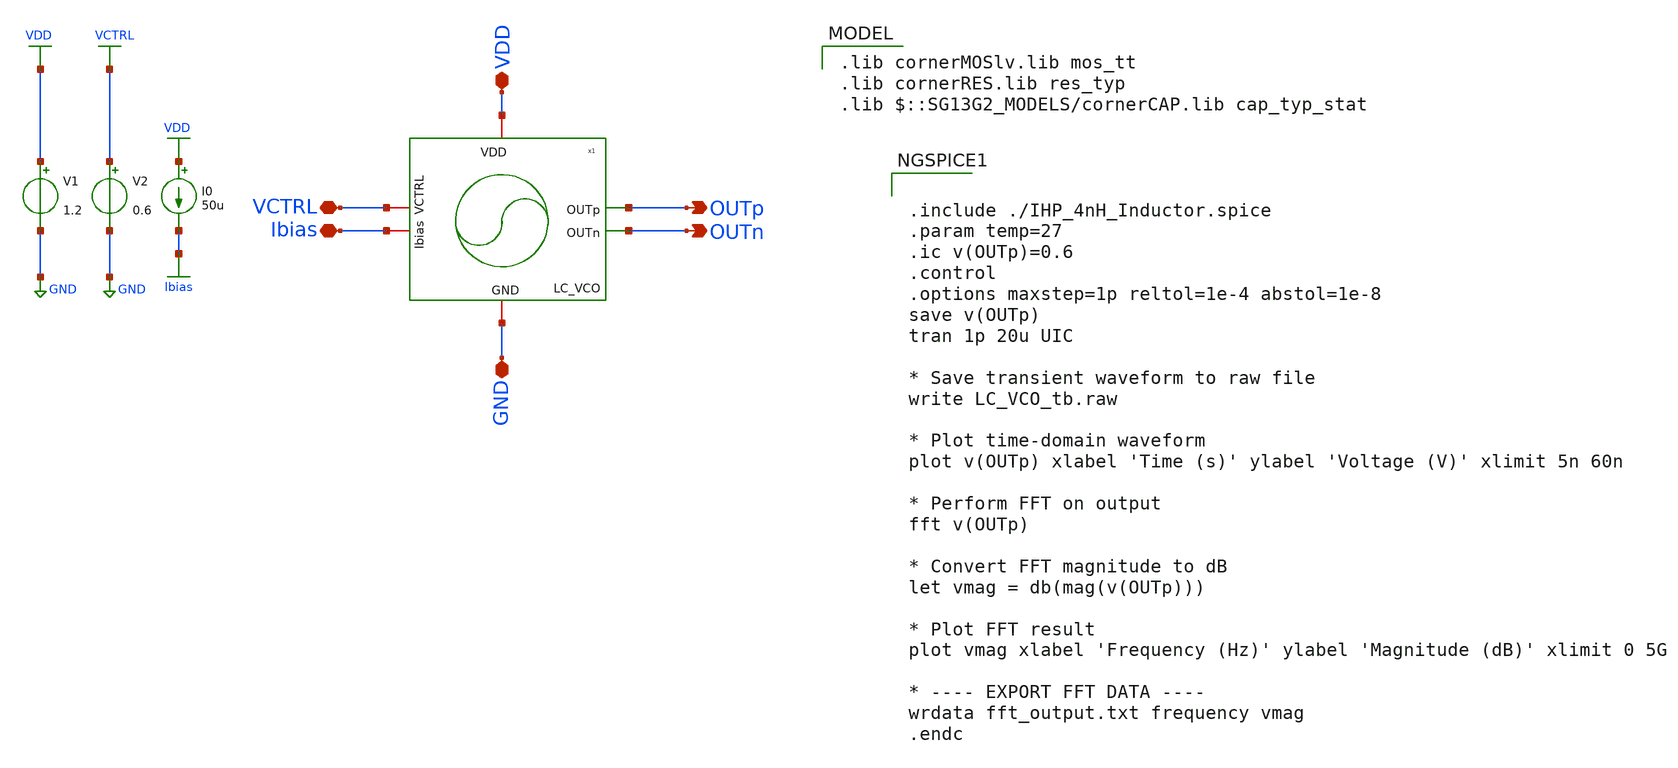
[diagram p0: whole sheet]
** sch_path: schematic/top-pll/lc-vco/LC_VCO_PN_tb.sch
**.subckt LC_VCO_PN_tb OUTp OUTn VDD VCTRL GND Ibias
*.opin OUTp
*.opin OUTn
*.iopin VDD
*.iopin VCTRL
*.iopin GND
*.iopin Ibias
V1 VDD GND 1.2
V2 VCTRL GND 0.6
I0 VDD Ibias 50u
x1 VDD OUTp OUTn Ibias VCTRL GND LC_VCO
**** begin user architecture code
 .lib cornerMOSlv.lib mos_tt
.lib cornerRES.lib res_typ
.lib $::SG13G2_MODELS/cornerCAP.lib cap_typ_stat



.include ./IHP_4nH_Inductor.spice
.param temp=27
.ic v(OUTp)=0.6
.control
.options maxstep=1p reltol=1e-4 abstol=1e-8
save v(OUTp)
tran 1p 20u UIC

* Save transient waveform to raw file
write LC_VCO_tb.raw

* Plot time-domain waveform
plot v(OUTp) xlabel 'Time (s)' ylabel 'Voltage (V)' xlimit 5n 60n

* Perform FFT on output
fft v(OUTp)

* Convert FFT magnitude to dB
let vmag = db(mag(v(OUTp)))

* Plot FFT result
plot vmag xlabel 'Frequency (Hz)' ylabel 'Magnitude (dB)' xlimit 0 5G

* ---- EXPORT FFT DATA ----
wrdata fft_output.txt frequency vmag
.endc


**** end user architecture code
**.ends
.GLOBAL GND
.GLOBAL VDD
.GLOBAL VCTRL
.GLOBAL Ibias
.end
